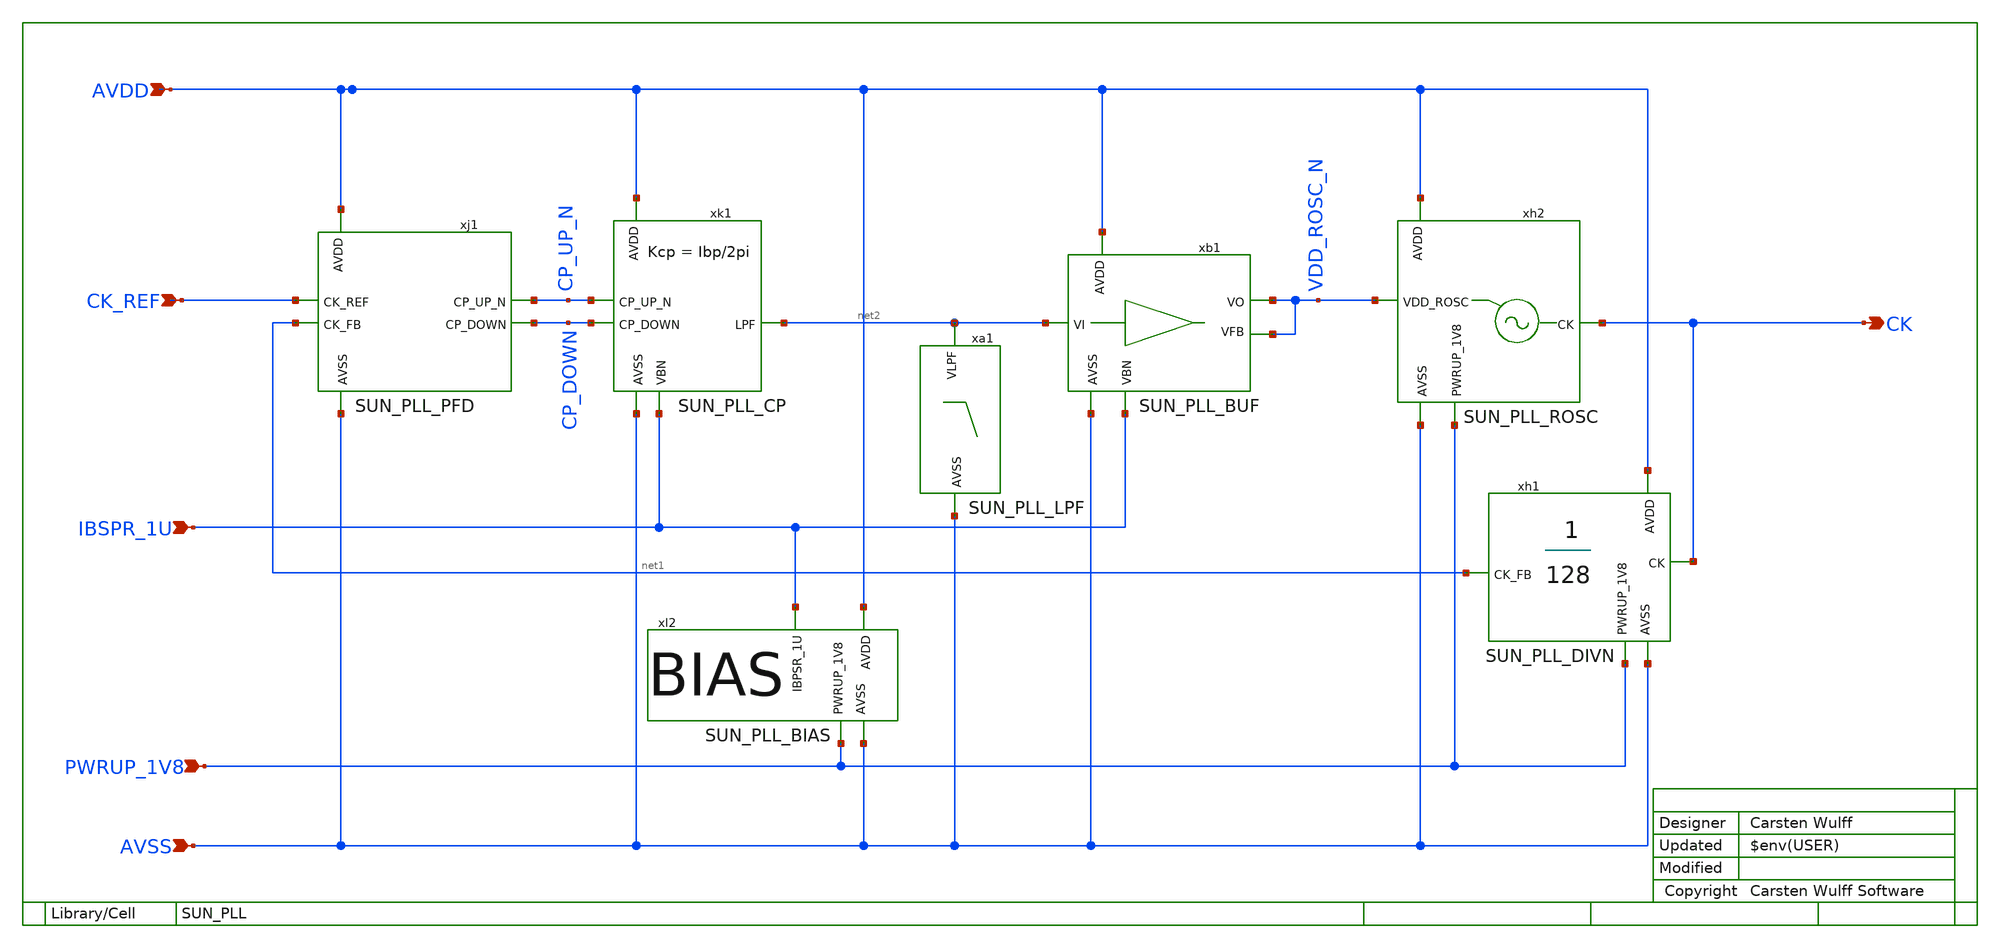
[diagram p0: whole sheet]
** sch_path: ip/sun_pll_sky130nm/design/SUN_PLL_SKY130NM/SUN_PLL.sch
**.subckt SUN_PLL AVDD AVSS PWRUP_1V8 CK_REF CK IBSPR_1U
*.ipin AVDD
*.ipin AVSS
*.ipin PWRUP_1V8
*.ipin CK_REF
*.opin CK
*.ipin IBSPR_1U
xh2 AVDD CK VDD_ROSC_N PWRUP_1V8 AVSS SUN_PLL_ROSC xoffset=0 yoffset=0 angle=0
xh1 AVDD net1 CK PWRUP_1V8 AVSS SUN_PLL_DIVN xoffset=4 yoffset=0 angle=0
xl2 IBSPR_1U AVDD PWRUP_1V8 AVSS SUN_PLL_BIAS xoffset=4 yoffset=80 angle=0
xb1 AVDD VDD_ROSC_N net2 VDD_ROSC_N IBSPR_1U AVSS SUN_PLL_BUF xoffset=4 yoffset=0 angle=0
xa1 net2 AVSS SUN_PLL_LPF xoffset=0 yoffset=0 angle=0
xk1 AVDD CP_UP_N net2 CP_DOWN IBSPR_1U AVSS SUN_PLL_CP xoffset=4 yoffset=80 angle=0
xj1 AVDD CP_UP_N CK_REF CP_DOWN net1 AVSS SUN_PLL_PFD xoffset=5 yoffset=80 angle=0
**.ends
.end
